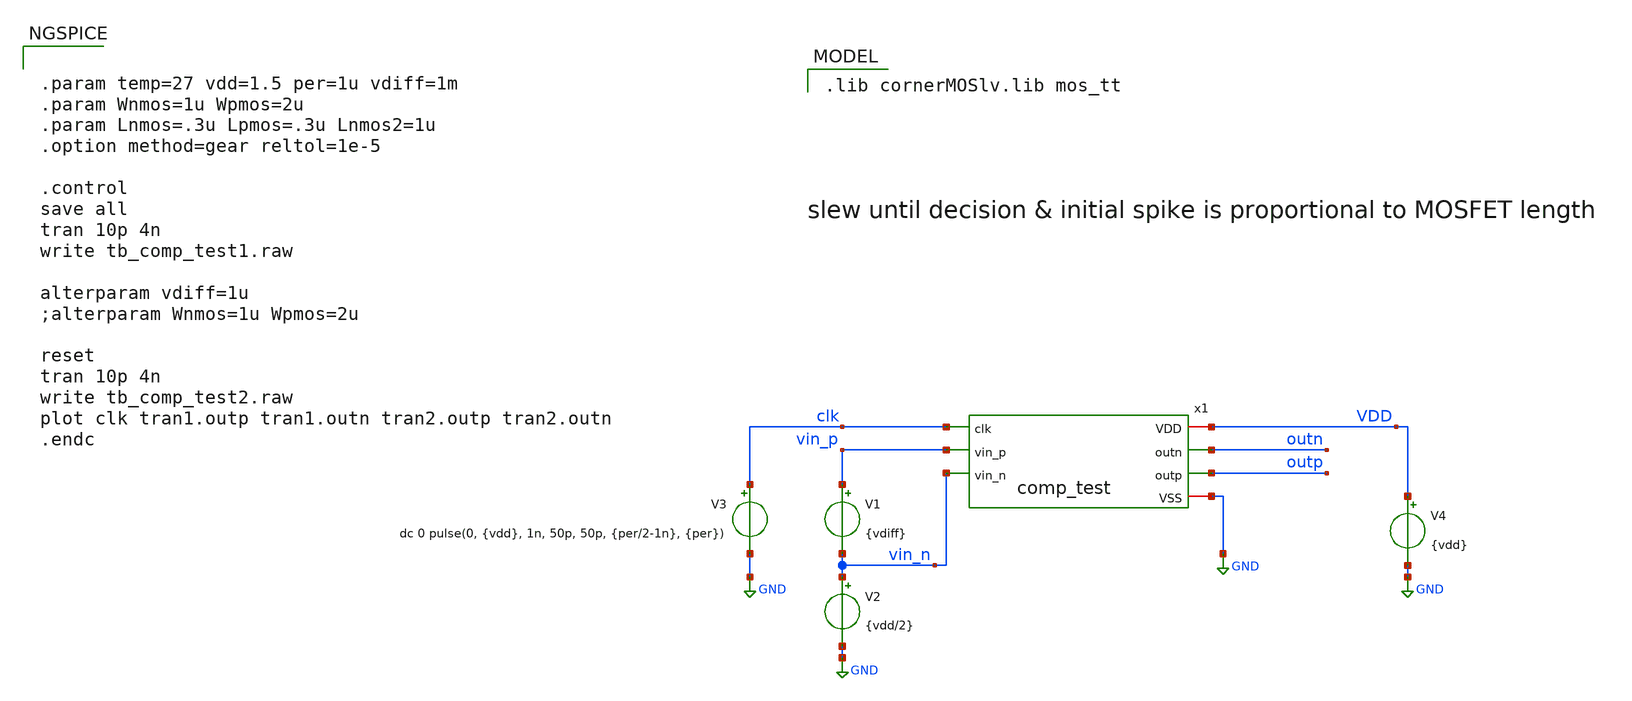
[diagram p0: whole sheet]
** sch_path: design/design_comp/tb_comp_test.sch
**.subckt tb_comp_test
x1 VDD clk outn outp vin_p vin_n GND comp_test
V1 vin_p vin_n {vdiff}
V2 vin_n GND {vdd/2}
V3 clk GND dc 0 pulse(0, {vdd}, 1n, 50p, 50p, {per/2-1n}, {per})
V4 VDD GND {vdd}
**** begin user architecture code
 .lib cornerMOSlv.lib mos_tt


.param temp=27 vdd=1.5 per=1u vdiff=1m
.param Wnmos=1u Wpmos=2u
.param Lnmos=.3u Lpmos=.3u Lnmos2=1u
.option method=gear reltol=1e-5

.control
save all
tran 10p 4n
write tb_comp_test1.raw

alterparam vdiff=1u
;alterparam Wnmos=1u Wpmos=2u

reset
tran 10p 4n
write tb_comp_test2.raw
plot clk tran1.outp tran1.outn tran2.outp tran2.outn
.endc

**** end user architecture code
**.ends

* expanding   symbol:  comp_test.sym # of pins=7
** sym_path: design/design_comp/comp_test.sym
** sch_path: design/design_comp/comp_test.sch
.subckt comp_test VDD clk outn outp vin_p vin_n VSS
*.ipin clk
*.iopin VSS
*.iopin VDD
*.ipin vin_n
*.ipin vin_p
*.opin outn
*.opin outp
XM5p outn clk VDD VDD sg13_lv_pmos w=Wpmos l=Lpmos ng=1 m=1 mm_ok=1
XM4n outp outn VDD VDD sg13_lv_pmos w=Wpmos l=Lpmos ng=1 m=1 mm_ok=1
XM4p outn outp VDD VDD sg13_lv_pmos w=Wpmos l=Lpmos ng=1 m=1 mm_ok=1
XM5n outp clk VDD VDD sg13_lv_pmos w=Wpmos l=Lpmos ng=1 m=1 mm_ok=1
XM3p d2p outp outn VSS sg13_lv_nmos w=Wnmos l=Lnmos ng=1 m=1 mm_ok=1
XM3n d2m outn outp VSS sg13_lv_nmos w=Wnmos l=Lnmos ng=1 m=1 mm_ok=1
XM2n d1m clk d2m VSS sg13_lv_nmos w=Wnmos l=Lnmos ng=1 m=1 mm_ok=1
XM2p d1p clk d2p VSS sg13_lv_nmos w=Wnmos l=Lnmos ng=1 m=1 mm_ok=1
XM1n VSS vin_n d1m VSS sg13_lv_nmos w=Wnmos l=Lnmos2 ng=1 m=1 mm_ok=1
XM1p VSS vin_p d1p VSS sg13_lv_nmos w=Wnmos l=Lnmos2 ng=1 m=1 mm_ok=1
.ends

.GLOBAL GND
.end
